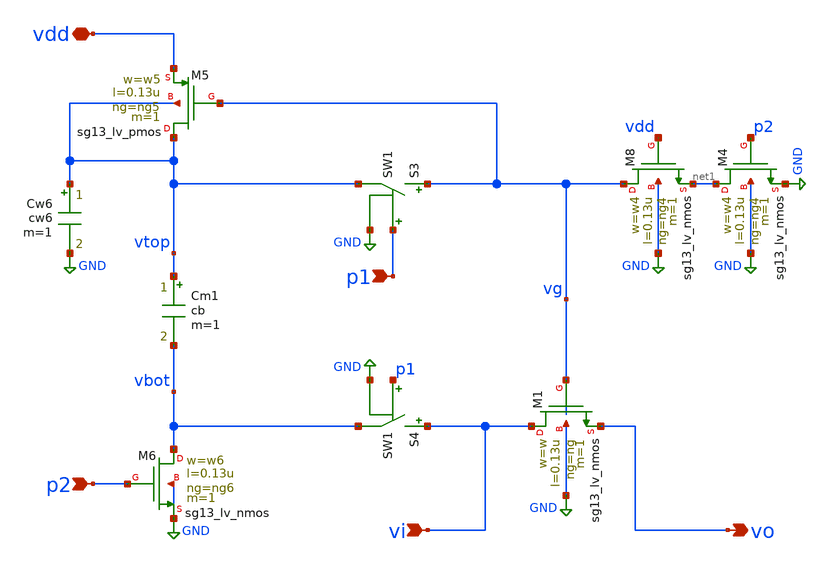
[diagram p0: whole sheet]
** sch_path: xschem/boot3.sch
**.subckt boot3 vi vo p2 vdd p1
*.ipin vi
*.opin vo
*.ipin p2
*.iopin vdd
*.ipin p1
Cm1 vtop vbot cb m=1
S4 vi vbot p1 GND SW1
XM1 vi vg vo GND sg13_lv_nmos w=w l=0.13u ng=ng m=1 mm_ok=1
XM8 vg vdd net1 GND sg13_lv_nmos w=w4 l=0.13u ng=ng4 m=1 mm_ok=1
XM4 net1 p2 GND GND sg13_lv_nmos w=w4 l=0.13u ng=ng4 m=1 mm_ok=1
XM6 vbot p2 GND GND sg13_lv_nmos w=w6 l=0.13u ng=ng6 m=1 mm_ok=1
XM5 vtop vg vdd vtop sg13_lv_pmos w=w5 l=0.13u ng=ng5 m=1 mm_ok=1
S3 vg vtop p1 GND SW1
Cw6 vtop GND cw6 m=1
**.ends
.GLOBAL GND
**** begin user architecture code
.MODEL SW1 SW   VT=0.6 VH=vh  RON=rsw ROFF=roff
**** end user architecture code
.end
